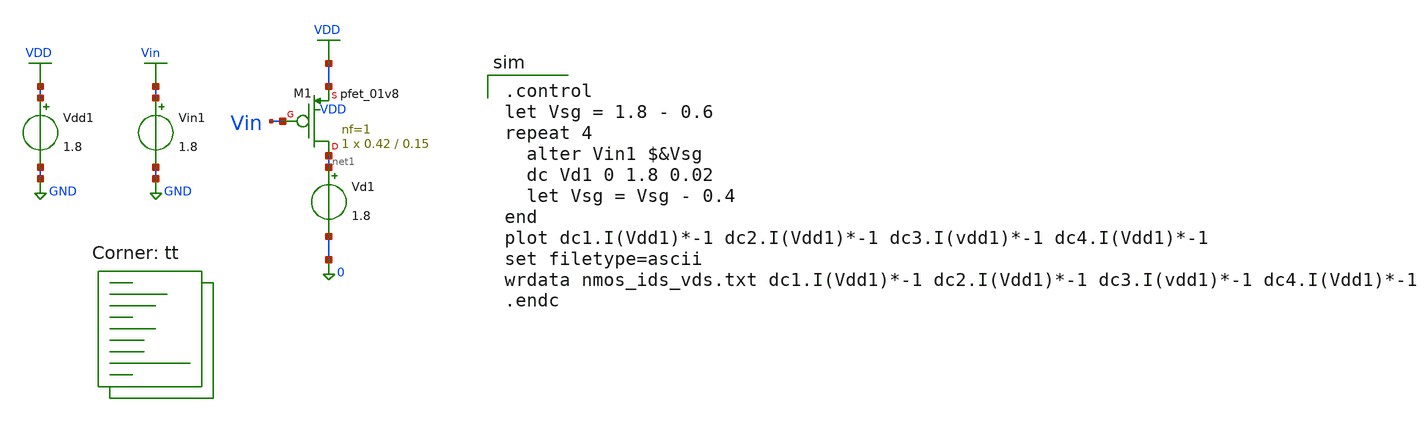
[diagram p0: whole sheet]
** sch_path: tutorial-1/source/q2b.sch
**.subckt q2b
Vdd1 VDD GND 1.8
Vin1 Vin GND 1.8
XM1 net1 Vin VDD VDD sky130_fd_pr__pfet_01v8 L=0.15 W=0.42 nf=1 ad='int((nf+1)/2) * W/nf * 0.29' as='int((nf+2)/2) * W/nf * 0.29'
+ pd='2*int((nf+1)/2) * (W/nf + 0.29)' ps='2*int((nf+2)/2) * (W/nf + 0.29)' nrd='0.29 / W' nrs='0.29 / W'
+ sa=0 sb=0 sd=0 mult=1 m=1
Vd1 net1 0 1.8
**** begin user architecture code
.lib $::SKYWATER_MODELS/sky130.lib.spice tt

.control
let Vsg = 1.8 - 0.6
repeat 4
  alter Vin1 $&Vsg
  dc Vd1 0 1.8 0.02
  let Vsg = Vsg - 0.4
end
plot dc1.I(Vdd1)*-1 dc2.I(Vdd1)*-1 dc3.I(vdd1)*-1 dc4.I(Vdd1)*-1
set filetype=ascii
wrdata nmos_ids_vds.txt dc1.I(Vdd1)*-1 dc2.I(Vdd1)*-1 dc3.I(vdd1)*-1 dc4.I(Vdd1)*-1
.endc

**** end user architecture code
**.ends
.GLOBAL VDD
.GLOBAL GND
.GLOBAL Vin
.end
